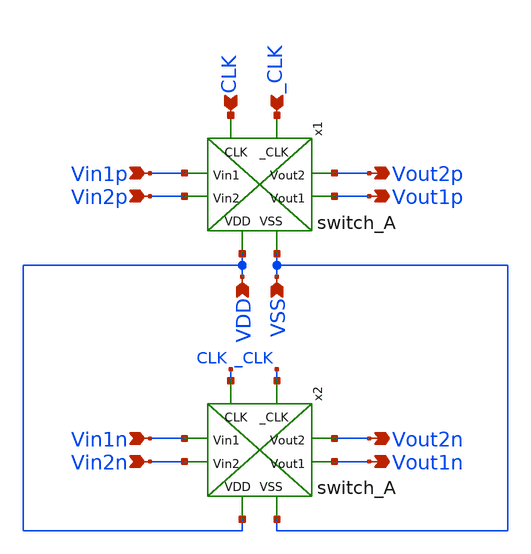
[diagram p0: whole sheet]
** sch_path: ISSCC26/submitted_notebooks/Low Mismatch 4 Channels Instrumentation Amplifier EEG/Chopper Switch/Schmatic and Testbench/switch_B.sch
**.subckt switch_B Vin1p Vin2p Vin1n Vin2n Vout1p Vout2p Vout1n Vout2n CLK _CLK VDD VSS
*.ipin Vin1p
*.ipin Vin2p
*.ipin Vin1n
*.ipin Vin2n
*.opin Vout1p
*.opin Vout2p
*.opin Vout1n
*.opin Vout2n
*.ipin CLK
*.ipin _CLK
*.ipin VDD
*.ipin VSS
x1 CLK _CLK Vin1p Vout2p Vout1p Vin2p VDD VSS switch_A
x2 CLK _CLK Vin1n Vout2n Vout1n Vin2n VDD VSS switch_A
**.ends
.end
